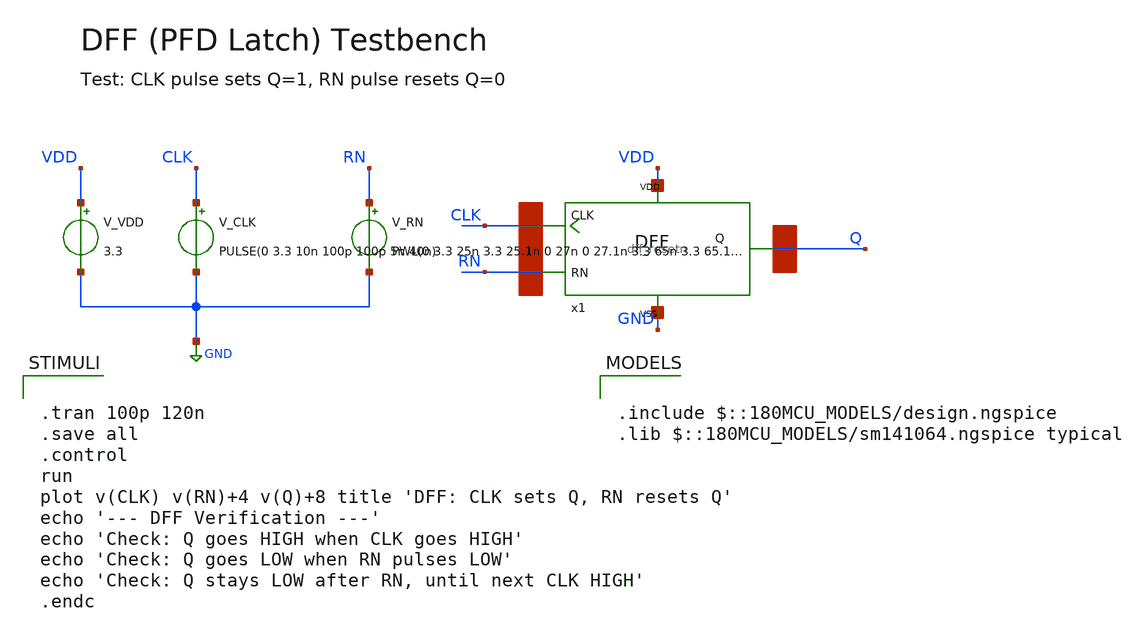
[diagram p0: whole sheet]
** sch_path: designs/libs/PDF/dff_resetn_tb.sch
**.subckt dff_resetn_tb
x1 CLK RN Q VDD GND dff_resetn
V_CLK CLK GND PULSE(0 3.3 10n 100p 100p 5n 40n)
V_RN RN GND PWL(0 3.3 25n 3.3 25.1n 0 27n 0 27.1n 3.3 65n 3.3 65.1n 0 67n 0 67.1n 3.3)
V_VDD VDD GND 3.3
**** begin user architecture code


.tran 100p 120n
.save all
.control
run
plot v(CLK) v(RN)+4 v(Q)+8 title 'DFF: CLK sets Q, RN resets Q'
echo '--- DFF Verification ---'
echo 'Check: Q goes HIGH when CLK goes HIGH'
echo 'Check: Q goes LOW when RN pulses LOW'
echo 'Check: Q stays LOW after RN, until next CLK HIGH'
.endc



.include $::180MCU_MODELS/design.ngspice
.lib $::180MCU_MODELS/sm141064.ngspice typical

**** end user architecture code
**.ends
.GLOBAL GND
.end
